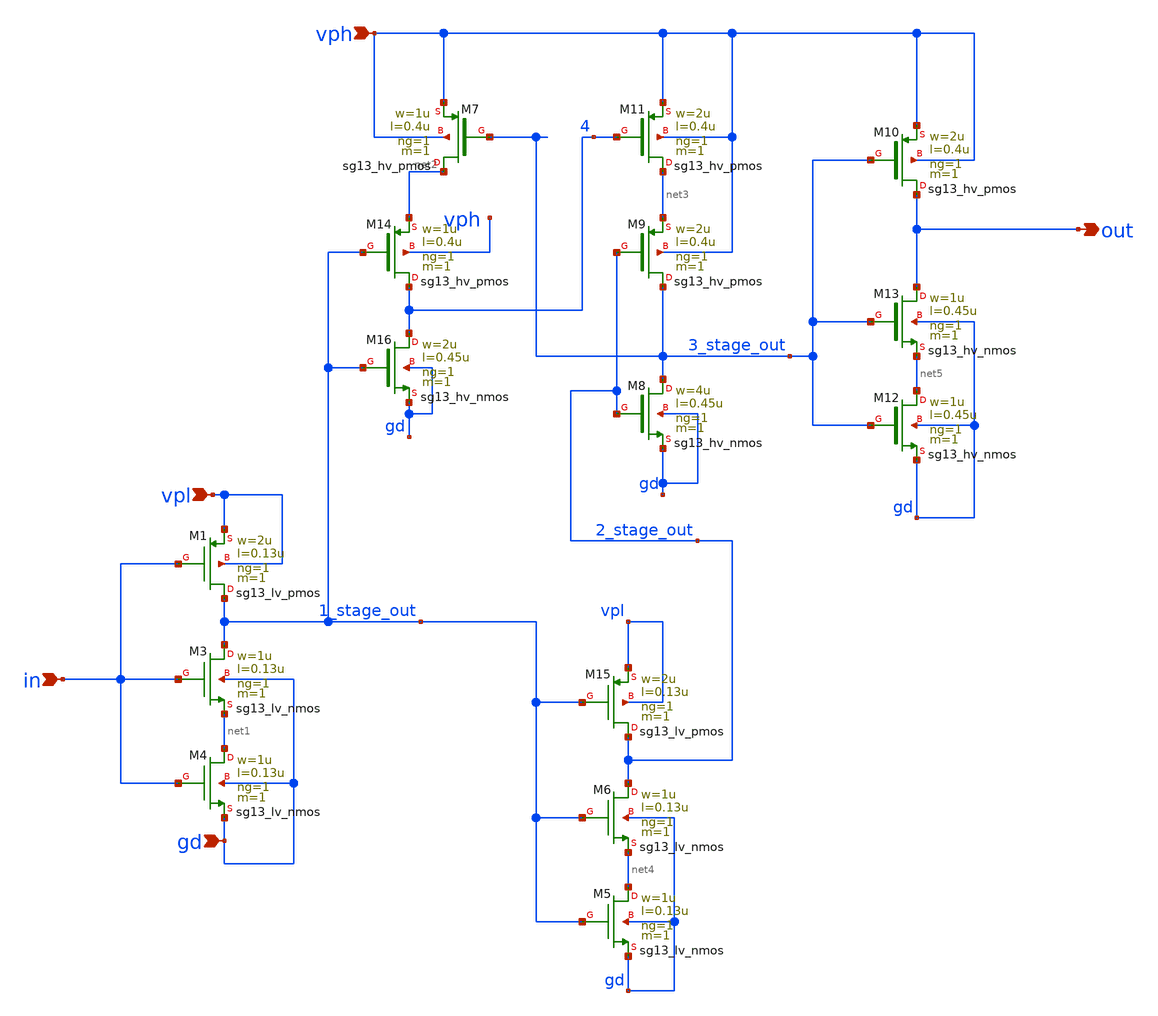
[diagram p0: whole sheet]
** sch_path: schematics/misc/level_shifter.sch
**.subckt level_shifter in out gd vph vpl
*.ipin in
*.opin out
*.ipin gd
*.ipin vph
*.ipin vpl
XM16 4 1_stage_out gd gd sg13_hv_nmos w=2u l=0.45u ng=1 m=1 mm_ok=1
XM8 3_stage_out 2_stage_out gd gd sg13_hv_nmos w=4u l=0.45u ng=1 m=1 mm_ok=1
XM12 net5 3_stage_out gd gd sg13_hv_nmos w=1u l=0.45u ng=1 m=1 mm_ok=1
XM13 out 3_stage_out net5 gd sg13_hv_nmos w=1u l=0.45u ng=1 m=1 mm_ok=1
XM14 4 1_stage_out net2 vph sg13_hv_pmos w=1u l=0.4u ng=1 m=1 mm_ok=1
XM9 3_stage_out 2_stage_out net3 vph sg13_hv_pmos w=2u l=0.4u ng=1 m=1 mm_ok=1
XM10 out 3_stage_out vph vph sg13_hv_pmos w=2u l=0.4u ng=1 m=1 mm_ok=1
XM11 net3 4 vph vph sg13_hv_pmos w=2u l=0.4u ng=1 m=1 mm_ok=1
XM7 net2 3_stage_out vph vph sg13_hv_pmos w=1u l=0.4u ng=1 m=1 mm_ok=1
XM3 1_stage_out in net1 gd sg13_lv_nmos w=1u l=0.13u ng=1 m=1 mm_ok=1
XM4 net1 in gd gd sg13_lv_nmos w=1u l=0.13u ng=1 m=1 mm_ok=1
XM5 net4 1_stage_out gd gd sg13_lv_nmos w=1u l=0.13u ng=1 m=1 mm_ok=1
XM6 2_stage_out 1_stage_out net4 gd sg13_lv_nmos w=1u l=0.13u ng=1 m=1 mm_ok=1
XM15 2_stage_out 1_stage_out vpl vpl sg13_lv_pmos w=2u l=0.13u ng=1 m=1 mm_ok=1
XM1 1_stage_out in vpl vpl sg13_lv_pmos w=2u l=0.13u ng=1 m=1 mm_ok=1
**.ends
.end
